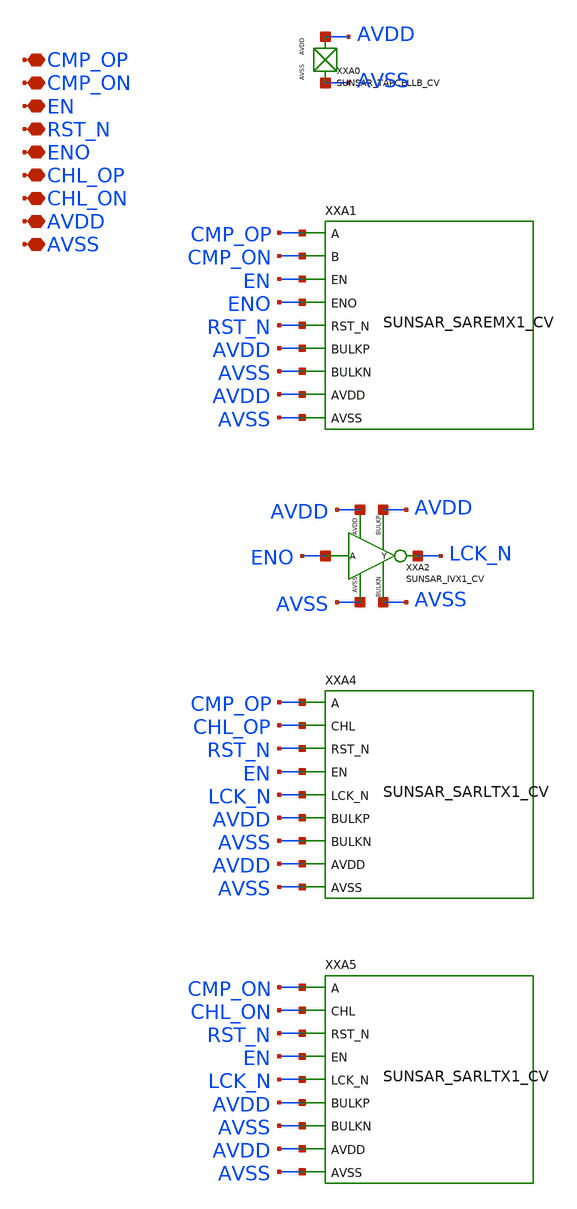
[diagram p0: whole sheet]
** sch_path: design/SUN_SAR9B_SKY130NM/SUNSAR_SARMRYX1_CV.sch
**.subckt SUNSAR_SARMRYX1_CV CMP_OP CMP_ON EN RST_N ENO CHL_OP CHL_ON AVDD AVSS
*.iopin CMP_OP
*.iopin CMP_ON
*.iopin EN
*.iopin RST_N
*.iopin ENO
*.iopin CHL_OP
*.iopin CHL_ON
*.iopin AVDD
*.iopin AVSS
XXA0 AVDD AVSS SUNSAR_TAPCELLB_CV
XXA1 CMP_OP CMP_ON EN ENO RST_N AVDD AVSS AVDD AVSS SUNSAR_SAREMX1_CV
XXA2 ENO LCK_N AVDD AVSS AVDD AVSS SUNSAR_IVX1_CV
XXA4 CMP_OP CHL_OP RST_N EN LCK_N AVDD AVSS AVDD AVSS SUNSAR_SARLTX1_CV
XXA5 CMP_ON CHL_ON RST_N EN LCK_N AVDD AVSS AVDD AVSS SUNSAR_SARLTX1_CV
**.ends
.end
